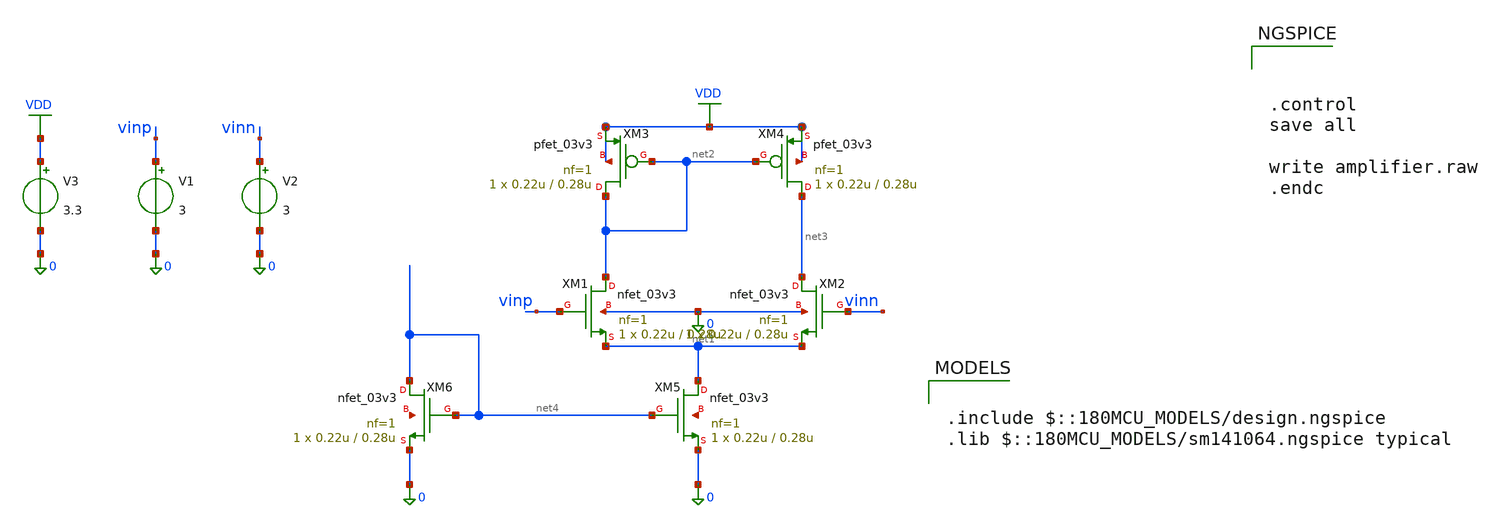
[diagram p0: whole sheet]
** sch_path: amplifier/untitled.sch
**.subckt untitled
XM1 net2 vinp net1 0 nfet_03v3 L=0.28u W=0.22u nf=1 ad='int((nf+1)/2) * W/nf * 0.18u' as='int((nf+2)/2) * W/nf * 0.18u'
+ pd='2*int((nf+1)/2) * (W/nf + 0.18u)' ps='2*int((nf+2)/2) * (W/nf + 0.18u)' nrd='0.18u / W' nrs='0.18u / W'
+ sa=0 sb=0 sd=0 m=1
XM2 net3 vinn net1 0 nfet_03v3 L=0.28u W=0.22u nf=1 ad='int((nf+1)/2) * W/nf * 0.18u' as='int((nf+2)/2) * W/nf * 0.18u'
+ pd='2*int((nf+1)/2) * (W/nf + 0.18u)' ps='2*int((nf+2)/2) * (W/nf + 0.18u)' nrd='0.18u / W' nrs='0.18u / W'
+ sa=0 sb=0 sd=0 m=1
XM3 net2 net2 VDD VDD pfet_03v3 L=0.28u W=0.22u nf=1 ad='int((nf+1)/2) * W/nf * 0.18u' as='int((nf+2)/2) * W/nf * 0.18u'
+ pd='2*int((nf+1)/2) * (W/nf + 0.18u)' ps='2*int((nf+2)/2) * (W/nf + 0.18u)' nrd='0.18u / W' nrs='0.18u / W'
+ sa=0 sb=0 sd=0 m=1
XM4 net3 net2 VDD VDD pfet_03v3 L=0.28u W=0.22u nf=1 ad='int((nf+1)/2) * W/nf * 0.18u' as='int((nf+2)/2) * W/nf * 0.18u'
+ pd='2*int((nf+1)/2) * (W/nf + 0.18u)' ps='2*int((nf+2)/2) * (W/nf + 0.18u)' nrd='0.18u / W' nrs='0.18u / W'
+ sa=0 sb=0 sd=0 m=1
XM5 net1 net4 0 net5 nfet_03v3 L=0.28u W=0.22u nf=1 ad='int((nf+1)/2) * W/nf * 0.18u' as='int((nf+2)/2) * W/nf * 0.18u'
+ pd='2*int((nf+1)/2) * (W/nf + 0.18u)' ps='2*int((nf+2)/2) * (W/nf + 0.18u)' nrd='0.18u / W' nrs='0.18u / W'
+ sa=0 sb=0 sd=0 m=1
XM6 net4 net4 0 net6 nfet_03v3 L=0.28u W=0.22u nf=1 ad='int((nf+1)/2) * W/nf * 0.18u' as='int((nf+2)/2) * W/nf * 0.18u'
+ pd='2*int((nf+1)/2) * (W/nf + 0.18u)' ps='2*int((nf+2)/2) * (W/nf + 0.18u)' nrd='0.18u / W' nrs='0.18u / W'
+ sa=0 sb=0 sd=0 m=1
V1 vinp 0 3
V2 vinn 0 3
V3 VDD 0 3.3
**** begin user architecture code

.include $::180MCU_MODELS/design.ngspice
.lib $::180MCU_MODELS/sm141064.ngspice typical




.control
save all

write amplifier.raw
.endc


**** end user architecture code
**.ends
.GLOBAL VDD
.end
